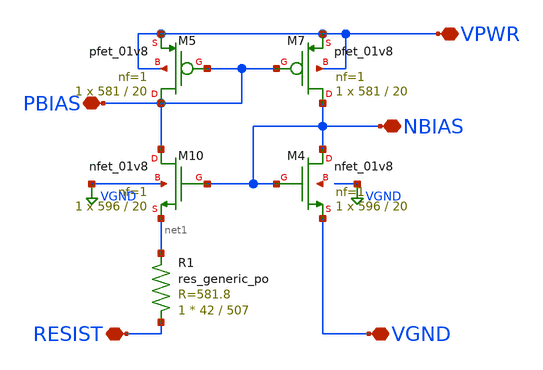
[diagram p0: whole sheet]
** sch_path: project2/sky130_hilas_Bootstrap01.sch
**.subckt sky130_hilas_Bootstrap01 VPWR NBIAS PBIAS VGND RESIST
*.iopin VPWR
*.iopin NBIAS
*.iopin PBIAS
*.iopin VGND
*.iopin RESIST
XM4 NBIAS NBIAS VGND net2 sky130_fd_pr__nfet_01v8 L=20 W=596 nf=1 ad='int((nf+1)/2) * W/nf * 0.29' as='int((nf+2)/2) * W/nf * 0.29'
+ pd='2*int((nf+1)/2) * (W/nf + 0.29)' ps='2*int((nf+2)/2) * (W/nf + 0.29)' nrd='0.29 / W' nrs='0.29 / W'
+ sa=0 sb=0 sd=0 mult=1 m=1
XM7 NBIAS PBIAS VPWR VPWR sky130_fd_pr__pfet_01v8 L=20 W=581 nf=1 ad='int((nf+1)/2) * W/nf * 0.29' as='int((nf+2)/2) * W/nf * 0.29'
+ pd='2*int((nf+1)/2) * (W/nf + 0.29)' ps='2*int((nf+2)/2) * (W/nf + 0.29)' nrd='0.29 / W' nrs='0.29 / W'
+ sa=0 sb=0 sd=0 mult=1 m=1
XM10 PBIAS NBIAS net1 VGND sky130_fd_pr__nfet_01v8 L=20 W=596 nf=1 ad='int((nf+1)/2) * W/nf * 0.29' as='int((nf+2)/2) * W/nf * 0.29'
+ pd='2*int((nf+1)/2) * (W/nf + 0.29)' ps='2*int((nf+2)/2) * (W/nf + 0.29)' nrd='0.29 / W' nrs='0.29 / W'
+ sa=0 sb=0 sd=0 mult=1 m=1
XM5 PBIAS PBIAS VPWR VPWR sky130_fd_pr__pfet_01v8 L=20 W=581 nf=1 ad='int((nf+1)/2) * W/nf * 0.29' as='int((nf+2)/2) * W/nf * 0.29'
+ pd='2*int((nf+1)/2) * (W/nf + 0.29)' ps='2*int((nf+2)/2) * (W/nf + 0.29)' nrd='0.29 / W' nrs='0.29 / W'
+ sa=0 sb=0 sd=0 mult=1 m=1
XR1 RESIST net1 sky130_fd_pr__res_generic_po W=42 L=507 m=1
**.ends
.GLOBAL VGND
.end
